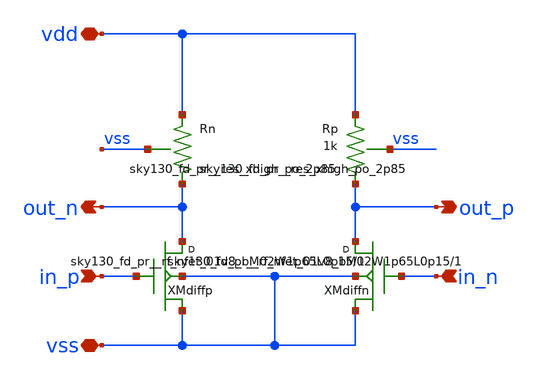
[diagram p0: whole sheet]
** sch_path: design/rf_bufferdiff/rf_bufferdiff.sch
**.subckt rf_bufferdiff vdd vss in_p in_n out_n out_p
*.iopin vdd
*.iopin vss
*.ipin in_p
*.ipin in_n
*.opin out_n
*.opin out_p
XXMdiffp out_n in_p vss vss sky130_fd_pr__rf_nfet_01v8_bM02W1p65L0p15 m=1
XXMdiffn out_p in_n vss vss sky130_fd_pr__rf_nfet_01v8_bM02W1p65L0p15 m=1
XRn vdd out_n vss sky130_fd_pr__res_xhigh_po_2p85 m=1
XRp vdd out_p vss sky130_fd_pr__res_xhigh_po_2p85 m=1
**.ends
.end
